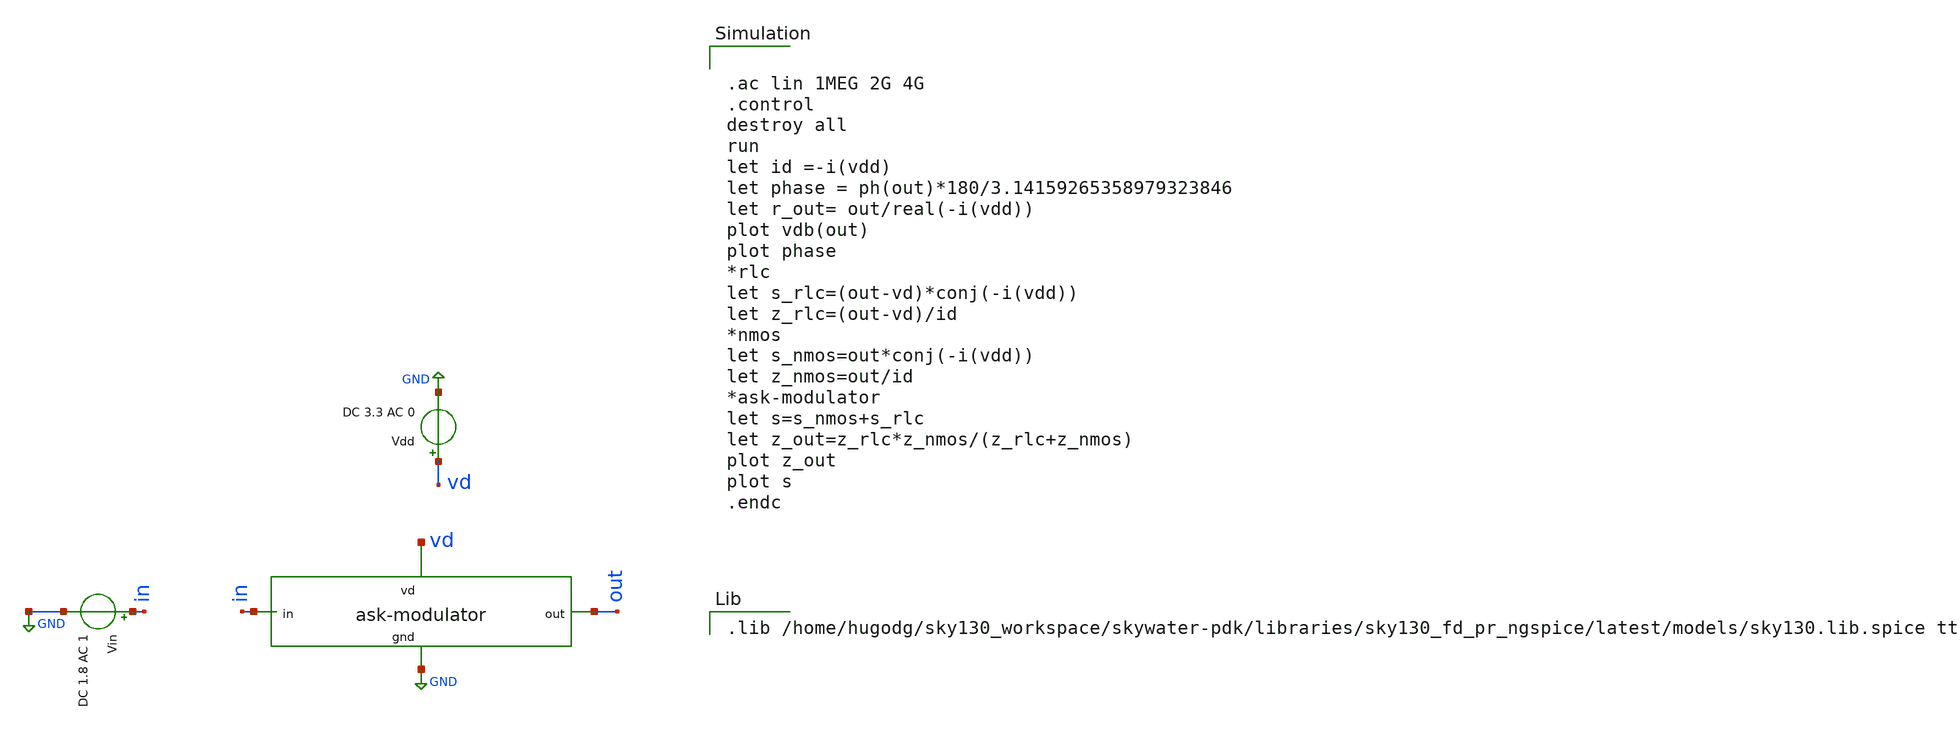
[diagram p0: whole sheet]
** sch_path: ask_modulator/xschem/ask-modulator_tb-ac.sch
**.subckt ask-modulator_tb-ac
Vdd vd GND DC 3.3 AC 0
Vin in GND DC 1.8 AC 1
x1 vd out in GND ask-modulator
**** begin user architecture code


.ac lin 1MEG 2G 4G
.control
destroy all
run
let id =-i(vdd)
let phase = ph(out)*180/3.14159265358979323846
let r_out= out/real(-i(vdd))
plot vdb(out)
plot phase
*rlc
let s_rlc=(out-vd)*conj(-i(vdd))
let z_rlc=(out-vd)/id
*nmos
let s_nmos=out*conj(-i(vdd))
let z_nmos=out/id
*ask-modulator
let s=s_nmos+s_rlc
let z_out=z_rlc*z_nmos/(z_rlc+z_nmos)
plot z_out
plot s
.endc


.lib /home/hugodg/sky130_workspace/skywater-pdk/libraries/sky130_fd_pr_ngspice/latest/models/sky130.lib.spice tt

**** end user architecture code
**.ends
.GLOBAL GND
.end
